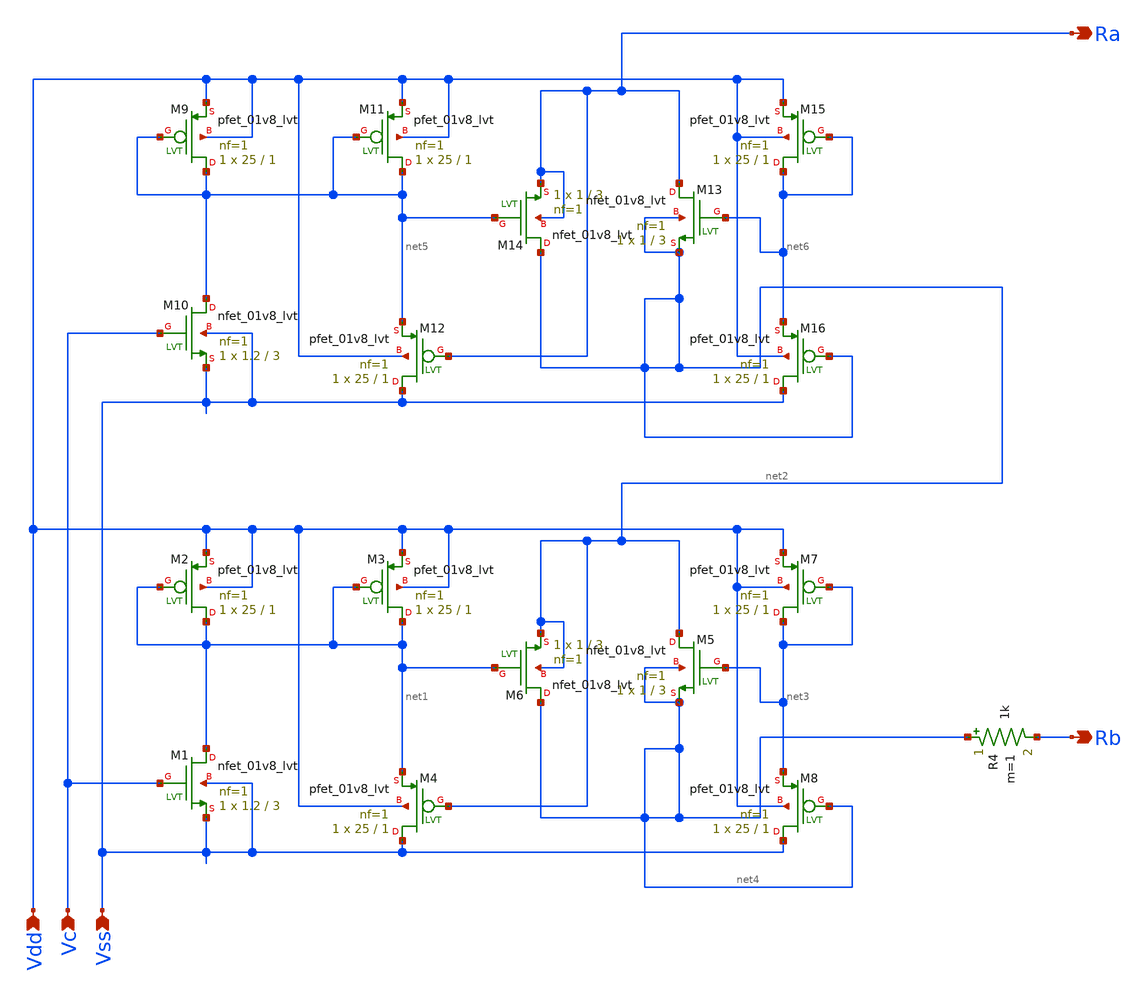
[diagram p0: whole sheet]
** sch_path: xschem/Active_Res_Low.sch
**.subckt Active_Res_Low Vss Vdd Vc Ra Rb
*.ipin Vss
*.ipin Vdd
*.ipin Vc
*.opin Ra
*.opin Rb
XM2 net1 net1 Vdd Vdd sky130_fd_pr__pfet_01v8_lvt L=1 W=25 nf=1 ad='int((1 + 1)/2) * 25 / 1 * 0.29' as='int((1 + 2)/2) * 25 / 1 * 0.29'
+ pd='2*int((1 + 1)/2) * (25 / 1 + 0.29)' ps='2*int((1 + 2)/2) * (25 / 1 + 0.29)' nrd='0.29 / 25 ' nrs='0.29 / 25 '
+ sa=0 sb=0 sd=0 mult=1 m=1
XM1 net1 Vc Vss Vss sky130_fd_pr__nfet_01v8_lvt L=3 W=1.2 nf=1 ad='int((1 + 1)/2) * 1.2 / 1 * 0.29' as='int((1 + 2)/2) * 1.2 / 1 * 0.29'
+ pd='2*int((1 + 1)/2) * (1.2 / 1 + 0.29)' ps='2*int((1 + 2)/2) * (1.2 / 1 + 0.29)' nrd='0.29 / 1.2 ' nrs='0.29 / 1.2 '
+ sa=0 sb=0 sd=0 mult=1 m=1
XM3 net1 net1 Vdd Vdd sky130_fd_pr__pfet_01v8_lvt L=1 W=25 nf=1 ad='int((1 + 1)/2) * 25 / 1 * 0.29' as='int((1 + 2)/2) * 25 / 1 * 0.29'
+ pd='2*int((1 + 1)/2) * (25 / 1 + 0.29)' ps='2*int((1 + 2)/2) * (25 / 1 + 0.29)' nrd='0.29 / 25 ' nrs='0.29 / 25 '
+ sa=0 sb=0 sd=0 mult=1 m=1
XM4 Vss net2 net1 Vdd sky130_fd_pr__pfet_01v8_lvt L=1 W=25 nf=1 ad='int((1 + 1)/2) * 25 / 1 * 0.29' as='int((1 + 2)/2) * 25 / 1 * 0.29'
+ pd='2*int((1 + 1)/2) * (25 / 1 + 0.29)' ps='2*int((1 + 2)/2) * (25 / 1 + 0.29)' nrd='0.29 / 25 ' nrs='0.29 / 25 '
+ sa=0 sb=0 sd=0 mult=1 m=1
XM5 net2 net3 net4 net4 sky130_fd_pr__nfet_01v8_lvt L=3 W=1 nf=1 ad='int((1 + 1)/2) * 1 / 1 * 0.29' as='int((1 + 2)/2) * 1 / 1 * 0.29'
+ pd='2*int((1 + 1)/2) * (1 / 1 + 0.29)' ps='2*int((1 + 2)/2) * (1 / 1 + 0.29)' nrd='0.29 / 1 ' nrs='0.29 / 1 '
+ sa=0 sb=0 sd=0 mult=1 m=1
XM6 net4 net1 net2 net2 sky130_fd_pr__nfet_01v8_lvt L=3 W=1 nf=1 ad='int((1 + 1)/2) * 1 / 1 * 0.29' as='int((1 + 2)/2) * 1 / 1 * 0.29'
+ pd='2*int((1 + 1)/2) * (1 / 1 + 0.29)' ps='2*int((1 + 2)/2) * (1 / 1 + 0.29)' nrd='0.29 / 1 ' nrs='0.29 / 1 '
+ sa=0 sb=0 sd=0 mult=1 m=1
XM7 net3 net3 Vdd Vdd sky130_fd_pr__pfet_01v8_lvt L=1 W=25 nf=1 ad='int((1 + 1)/2) * 25 / 1 * 0.29' as='int((1 + 2)/2) * 25 / 1 * 0.29'
+ pd='2*int((1 + 1)/2) * (25 / 1 + 0.29)' ps='2*int((1 + 2)/2) * (25 / 1 + 0.29)' nrd='0.29 / 25 ' nrs='0.29 / 25 '
+ sa=0 sb=0 sd=0 mult=1 m=1
XM8 Vss net4 net3 Vdd sky130_fd_pr__pfet_01v8_lvt L=1 W=25 nf=1 ad='int((1 + 1)/2) * 25 / 1 * 0.29' as='int((1 + 2)/2) * 25 / 1 * 0.29'
+ pd='2*int((1 + 1)/2) * (25 / 1 + 0.29)' ps='2*int((1 + 2)/2) * (25 / 1 + 0.29)' nrd='0.29 / 25 ' nrs='0.29 / 25 '
+ sa=0 sb=0 sd=0 mult=1 m=1
XM9 net5 net5 Vdd Vdd sky130_fd_pr__pfet_01v8_lvt L=1 W=25 nf=1 ad='int((1 + 1)/2) * 25 / 1 * 0.29' as='int((1 + 2)/2) * 25 / 1 * 0.29'
+ pd='2*int((1 + 1)/2) * (25 / 1 + 0.29)' ps='2*int((1 + 2)/2) * (25 / 1 + 0.29)' nrd='0.29 / 25 ' nrs='0.29 / 25 '
+ sa=0 sb=0 sd=0 mult=1 m=1
XM10 net5 Vc Vss Vss sky130_fd_pr__nfet_01v8_lvt L=3 W=1.2 nf=1 ad='int((1 + 1)/2) * 1.2 / 1 * 0.29'
+ as='int((1 + 2)/2) * 1.2 / 1 * 0.29' pd='2*int((1 + 1)/2) * (1.2 / 1 + 0.29)' ps='2*int((1 + 2)/2) * (1.2 / 1 + 0.29)'
+ nrd='0.29 / 1.2 ' nrs='0.29 / 1.2 ' sa=0 sb=0 sd=0 mult=1 m=1
XM11 net5 net5 Vdd Vdd sky130_fd_pr__pfet_01v8_lvt L=1 W=25 nf=1 ad='int((1 + 1)/2) * 25 / 1 * 0.29'
+ as='int((1 + 2)/2) * 25 / 1 * 0.29' pd='2*int((1 + 1)/2) * (25 / 1 + 0.29)' ps='2*int((1 + 2)/2) * (25 / 1 + 0.29)'
+ nrd='0.29 / 25 ' nrs='0.29 / 25 ' sa=0 sb=0 sd=0 mult=1 m=1
XM12 Vss Ra net5 Vdd sky130_fd_pr__pfet_01v8_lvt L=1 W=25 nf=1 ad='int((1 + 1)/2) * 25 / 1 * 0.29' as='int((1 + 2)/2) * 25 / 1 * 0.29'
+ pd='2*int((1 + 1)/2) * (25 / 1 + 0.29)' ps='2*int((1 + 2)/2) * (25 / 1 + 0.29)' nrd='0.29 / 25 ' nrs='0.29 / 25 '
+ sa=0 sb=0 sd=0 mult=1 m=1
XM13 Ra net6 net2 net2 sky130_fd_pr__nfet_01v8_lvt L=3 W=1 nf=1 ad='int((1 + 1)/2) * 1 / 1 * 0.29' as='int((1 + 2)/2) * 1 / 1 * 0.29'
+ pd='2*int((1 + 1)/2) * (1 / 1 + 0.29)' ps='2*int((1 + 2)/2) * (1 / 1 + 0.29)' nrd='0.29 / 1 ' nrs='0.29 / 1 '
+ sa=0 sb=0 sd=0 mult=1 m=1
XM14 net2 net5 Ra Ra sky130_fd_pr__nfet_01v8_lvt L=3 W=1 nf=1 ad='int((1 + 1)/2) * 1 / 1 * 0.29' as='int((1 + 2)/2) * 1 / 1 * 0.29'
+ pd='2*int((1 + 1)/2) * (1 / 1 + 0.29)' ps='2*int((1 + 2)/2) * (1 / 1 + 0.29)' nrd='0.29 / 1 ' nrs='0.29 / 1 '
+ sa=0 sb=0 sd=0 mult=1 m=1
XM15 net6 net6 Vdd Vdd sky130_fd_pr__pfet_01v8_lvt L=1 W=25 nf=1 ad='int((1 + 1)/2) * 25 / 1 * 0.29'
+ as='int((1 + 2)/2) * 25 / 1 * 0.29' pd='2*int((1 + 1)/2) * (25 / 1 + 0.29)' ps='2*int((1 + 2)/2) * (25 / 1 + 0.29)'
+ nrd='0.29 / 25 ' nrs='0.29 / 25 ' sa=0 sb=0 sd=0 mult=1 m=1
XM16 Vss net2 net6 Vdd sky130_fd_pr__pfet_01v8_lvt L=1 W=25 nf=1 ad='int((1 + 1)/2) * 25 / 1 * 0.29'
+ as='int((1 + 2)/2) * 25 / 1 * 0.29' pd='2*int((1 + 1)/2) * (25 / 1 + 0.29)' ps='2*int((1 + 2)/2) * (25 / 1 + 0.29)'
+ nrd='0.29 / 25 ' nrs='0.29 / 25 ' sa=0 sb=0 sd=0 mult=1 m=1
R4 net4 Rb 1k m=1
**.ends
.end
